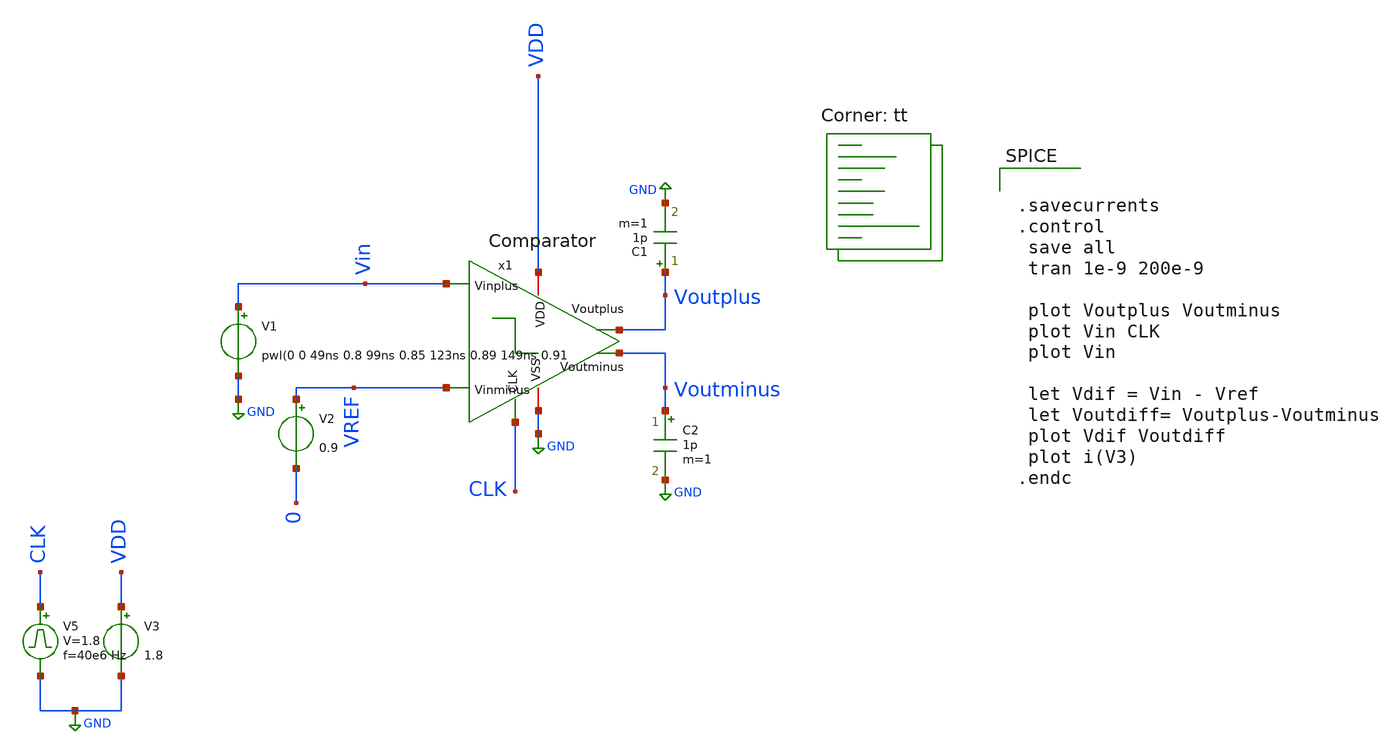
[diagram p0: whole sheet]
** sch_path: xschem/to_send/ComparatorTB.sch
**.subckt ComparatorTB
V2 VREF 0 0.9
V3 VDD GND 1.8
.save i(v3)
V1 Vin GND pwl(0 0 49ns 0.8 99ns 0.85 123ns 0.89 149ns 0.91
C1 Voutplus GND 1p m=1
C2 Voutminus GND 1p m=1
V5 CLK GND pulse 0 1.8 '0.495/ 40e6 ' '0.01/40e6 ' '0.01/40e6 ' '0.49/40e6 ' '1/40e6 '
x1 VDD Voutminus Voutplus CLK Vin VREF GND Comparator
**** begin user architecture code


.savecurrents
.control
 save all
 tran 1e-9 200e-9

 plot Voutplus Voutminus
 plot Vin CLK
 plot Vin

 let Vdif = Vin - Vref
 let Voutdiff= Voutplus-Voutminus
 plot Vdif Voutdiff
 plot i(V3)
.endc


.lib $::SKYWATER_MODELS/sky130.lib.spice tt
**** end user architecture code
**.ends
.GLOBAL GND
.end
